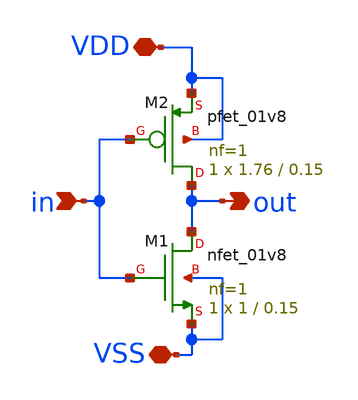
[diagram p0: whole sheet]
** sch_path: xschem/src/inverter.sch
**.subckt inverter in out VSS VDD
*.ipin in
*.opin out
*.iopin VSS
*.iopin VDD
XM1 out in VSS VSS sky130_fd_pr__nfet_01v8 L=0.15 W=1 nf=1 ad='int((nf+1)/2) * W/nf * 0.29' as='int((nf+2)/2) * W/nf * 0.29'
+ pd='2*int((nf+1)/2) * (W/nf + 0.29)' ps='2*int((nf+2)/2) * (W/nf + 0.29)' nrd='0.29 / W' nrs='0.29 / W'
+ sa=0 sb=0 sd=0 mult=1 m=1
XM2 out in VDD VDD sky130_fd_pr__pfet_01v8 L=0.15 W=1.76 nf=1 ad='int((nf+1)/2) * W/nf * 0.29' as='int((nf+2)/2) * W/nf * 0.29'
+ pd='2*int((nf+1)/2) * (W/nf + 0.29)' ps='2*int((nf+2)/2) * (W/nf + 0.29)' nrd='0.29 / W' nrs='0.29 / W'
+ sa=0 sb=0 sd=0 mult=1 m=1
**.ends
.end
